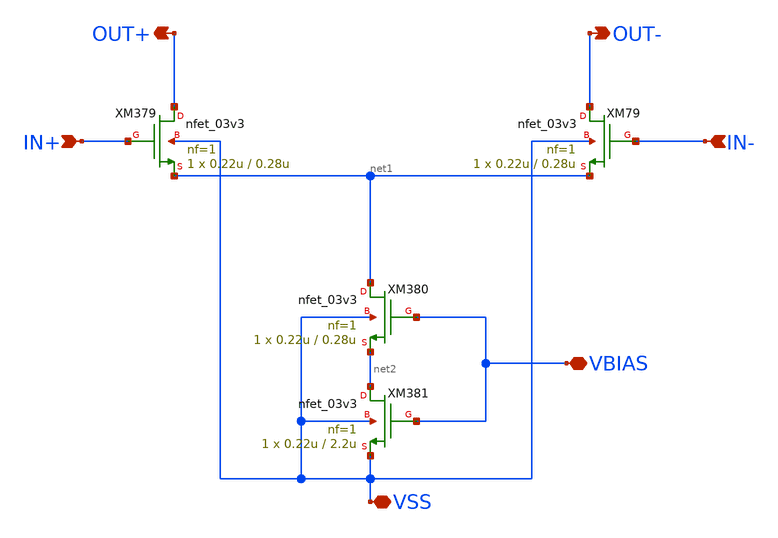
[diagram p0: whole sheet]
** sch_path: xschem/CS_Switch_1x.sch
**.subckt CS_Switch_1x VBIAS IN+ VSS IN- OUT+ OUT-
*.iopin VBIAS
*.ipin IN+
*.iopin VSS
*.ipin IN-
*.opin OUT+
*.opin OUT-
XM79 OUT- IN- net1 VSS nfet_03v3 L=0.28u W=0.22u nf=1 ad='int((nf+1)/2) * W/nf * 0.18u' as='int((nf+2)/2) * W/nf * 0.18u'
+ pd='2*int((nf+1)/2) * (W/nf + 0.18u)' ps='2*int((nf+2)/2) * (W/nf + 0.18u)' nrd='0.18u / W' nrs='0.18u / W'
+ sa=0 sb=0 sd=0 m=1
XM379 OUT+ IN+ net1 VSS nfet_03v3 L=0.28u W=0.22u nf=1 ad='int((nf+1)/2) * W/nf * 0.18u' as='int((nf+2)/2) * W/nf * 0.18u'
+ pd='2*int((nf+1)/2) * (W/nf + 0.18u)' ps='2*int((nf+2)/2) * (W/nf + 0.18u)' nrd='0.18u / W' nrs='0.18u / W'
+ sa=0 sb=0 sd=0 m=1
XM380 net1 VBIAS net2 VSS nfet_03v3 L=0.28u W=0.22u nf=1 ad='int((nf+1)/2) * W/nf * 0.18u' as='int((nf+2)/2) * W/nf * 0.18u'
+ pd='2*int((nf+1)/2) * (W/nf + 0.18u)' ps='2*int((nf+2)/2) * (W/nf + 0.18u)' nrd='0.18u / W' nrs='0.18u / W'
+ sa=0 sb=0 sd=0 m=1
XM381 net2 VBIAS VSS VSS nfet_03v3 L=2.2u W=0.22u nf=1 ad='int((nf+1)/2) * W/nf * 0.18u' as='int((nf+2)/2) * W/nf * 0.18u'
+ pd='2*int((nf+1)/2) * (W/nf + 0.18u)' ps='2*int((nf+2)/2) * (W/nf + 0.18u)' nrd='0.18u / W' nrs='0.18u / W'
+ sa=0 sb=0 sd=0 m=1
**.ends
.end
